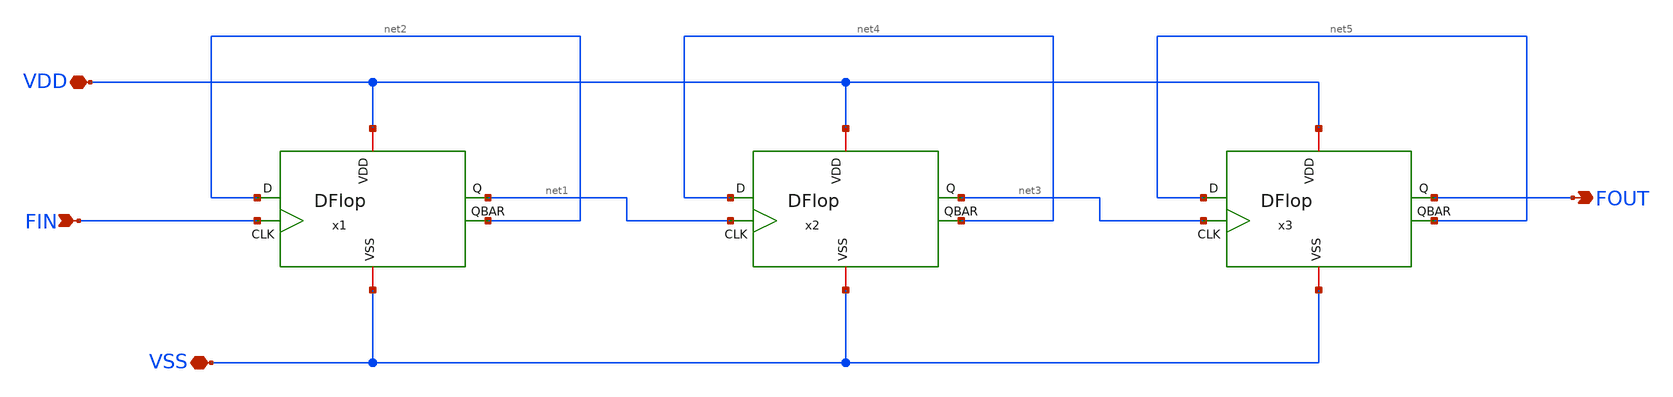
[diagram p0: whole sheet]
** sch_path: Team 1 Design/design_data/xschem/FD(Frequency_Dividers)/Div8F/Div8F.sch
**.subckt Div8F FOUT FIN VDD VSS
*.opin FOUT
*.ipin FIN
*.iopin VDD
*.iopin VSS
x1 VDD net2 net1 FIN net2 VSS DFlop
x2 VDD net4 net3 net1 net4 VSS DFlop
x3 VDD net5 FOUT net3 net5 VSS DFlop
**.ends
.end
